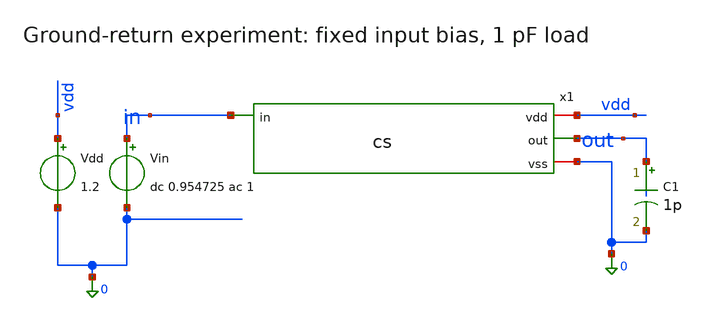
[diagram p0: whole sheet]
** sch_path: ISSCC27/submitted_notebooks/PerfPDN/examples/common_source_amplifier/cs_tb.sch
**.subckt cs_tb
x1 vdd out in 0 cs
Vin in 0 dc 0.954725 ac 1
C1 out 0 1p m=1
Vdd vdd 0 1.2
**** begin user architecture code
 .lib $::SKYWATER_MODELS/sky130.lib.spice tt


.option scale=1e-6 reltol=1e-8 abstol=1e-14
.temp 27
.control
op
ac dec 100 1k 10G
let gain_db=db(v(out))
wrdata cs_ac.txt gain_db
.endc


**** end user architecture code
**.ends

* expanding   symbol:  cs.sym # of pins=4
** sym_path: ISSCC27/submitted_notebooks/PerfPDN/examples/common_source_amplifier/cs.sym
** sch_path: ISSCC27/submitted_notebooks/PerfPDN/examples/common_source_amplifier/cs.sch
.subckt cs vdd out in vss
*.iopin vdd
*.iopin vss
*.ipin in
*.opin out
XR1 out vdd vss sky130_fd_pr__res_high_po_0p35 L=8.67 mult=1 m=1
XM1 out in vss vss sky130_fd_pr__nfet_01v8_lvt L=0.235 W=0.865 nf=1 ad='int(( 1 + 1 ) / 2 ) * 0.865 / 1 * 0.29'
+ as='int(( 1 + 2 ) / 2 ) * 0.865 / 1 * 0.29' pd='2 * int(( 1 + 1 ) / 2 ) * ( 0.865 / 1 + 0.29 )' ps='2 * int(( 1 + 2 ) / 2 ) * ( 0.865 / 1 + 0.29 )'
+ nrd='0.29 / 0.865 ' nrs='0.29 / 0.865 ' sa=0 sb=0 sd=0 mult=1 m=1
.ends

.end
